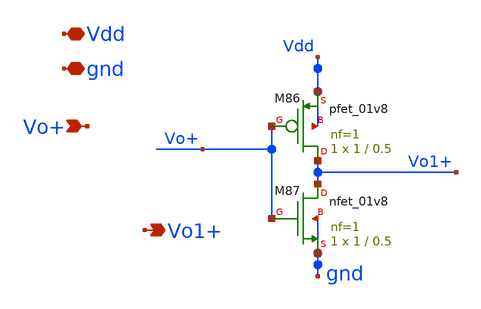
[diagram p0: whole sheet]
** sch_path: xschem/charge_pumps2/comparator_inv.sch
**.subckt comparator_inv gnd Vdd Vo+ Vo1+
*.iopin gnd
*.iopin Vdd
*.ipin Vo+
*.opin Vo1+
XM86 Vo1+ Vo+ Vdd Vdd sky130_fd_pr__pfet_01v8 L=0.5 W=1 nf=1 ad='int((nf+1)/2) * W/nf * 0.29' as='int((nf+2)/2) * W/nf * 0.29'
+ pd='2*int((nf+1)/2) * (W/nf + 0.29)' ps='2*int((nf+2)/2) * (W/nf + 0.29)' nrd='0.29 / W' nrs='0.29 / W'
+ sa=0 sb=0 sd=0 mult=1 m=1
XM87 Vo1+ Vo+ gnd gnd sky130_fd_pr__nfet_01v8 L=0.5 W=1 nf=1 ad='int((nf+1)/2) * W/nf * 0.29' as='int((nf+2)/2) * W/nf * 0.29'
+ pd='2*int((nf+1)/2) * (W/nf + 0.29)' ps='2*int((nf+2)/2) * (W/nf + 0.29)' nrd='0.29 / W' nrs='0.29 / W'
+ sa=0 sb=0 sd=0 mult=1 m=1
**.ends
.end
